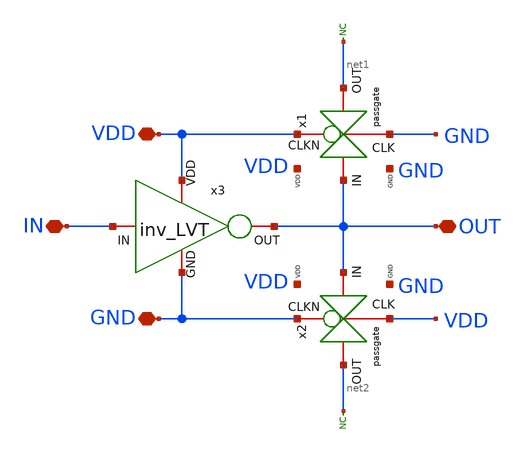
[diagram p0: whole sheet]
** sch_path: LVT/rovcel2_LVT.sch
**.subckt rovcel2_LVT OUT IN VDD GND
*.iopin OUT
*.iopin IN
*.iopin VDD
*.iopin GND
* noconn #net1
* noconn #net2
x1 VDD OUT net1 GND GND VDD passgate
x2 GND OUT net2 VDD GND VDD passgate
x3 VDD IN OUT GND inv_LVT
**.ends
.GLOBAL VDD
.GLOBAL GND
.end
